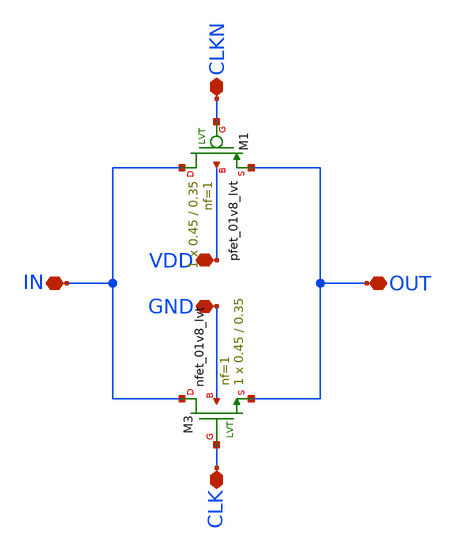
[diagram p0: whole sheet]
** sch_path: LVT/passgate_LVT/passgate_LVT.sch
**.subckt passgate_LVT CLKN CLK IN OUT VDD GND
*.iopin CLKN
*.iopin CLK
*.iopin IN
*.iopin OUT
*.iopin VDD
*.iopin GND
XM3 IN CLK OUT GND sky130_fd_pr__nfet_01v8_lvt L=0.35 W=0.45 nf=1 ad='int((nf+1)/2) * W/nf * 0.29' as='int((nf+2)/2) * W/nf * 0.29'
+ pd='2*int((nf+1)/2) * (W/nf + 0.29)' ps='2*int((nf+2)/2) * (W/nf + 0.29)' nrd='0.29 / W' nrs='0.29 / W'
+ sa=0 sb=0 sd=0 mult=1 m=1
XM1 IN CLKN OUT VDD sky130_fd_pr__pfet_01v8_lvt L=0.35 W=0.45 nf=1 ad='int((nf+1)/2) * W/nf * 0.29' as='int((nf+2)/2) * W/nf * 0.29'
+ pd='2*int((nf+1)/2) * (W/nf + 0.29)' ps='2*int((nf+2)/2) * (W/nf + 0.29)' nrd='0.29 / W' nrs='0.29 / W'
+ sa=0 sb=0 sd=0 mult=1 m=1
**.ends
.end
